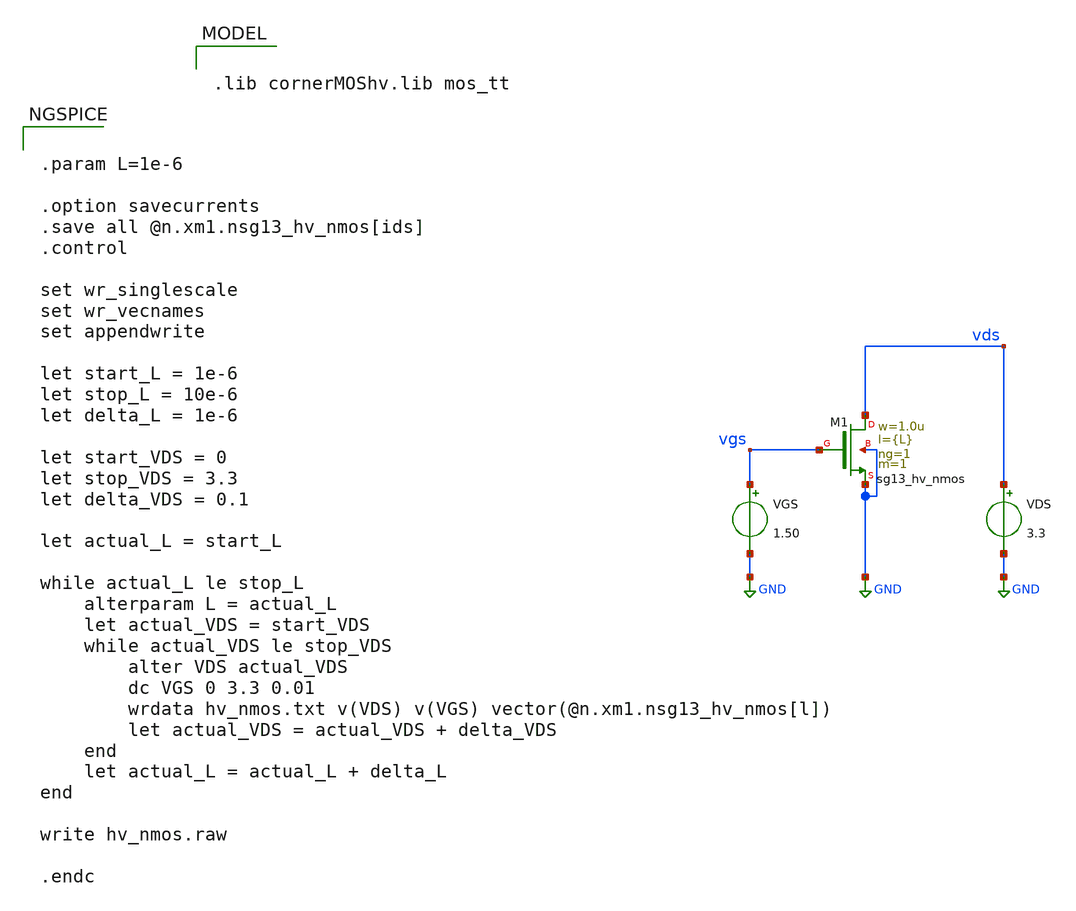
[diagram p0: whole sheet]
** sch_path: gmid/hv_nmos.sch
**.subckt hv_nmos
XM1 vds vgs GND GND sg13_hv_nmos w=1.0u l={L} ng=1 m=1 mm_ok=1
VGS vgs GND 1.50
VDS vds GND 3.3
**** begin user architecture code

.lib cornerMOShv.lib mos_tt



.param L=1e-6

.option savecurrents
.save all @n.xm1.nsg13_hv_nmos[ids]
.control

set wr_singlescale
set wr_vecnames
set appendwrite

let start_L = 1e-6
let stop_L = 10e-6
let delta_L = 1e-6

let start_VDS = 0
let stop_VDS = 3.3
let delta_VDS = 0.1

let actual_L = start_L

while actual_L le stop_L
	alterparam L = actual_L
	let actual_VDS = start_VDS
	while actual_VDS le stop_VDS
		alter VDS actual_VDS
		dc VGS 0 3.3 0.01
		wrdata hv_nmos.txt v(VDS) v(VGS) vector(@n.xm1.nsg13_hv_nmos[l])
		let actual_VDS = actual_VDS + delta_VDS
	end
	let actual_L = actual_L + delta_L
end

write hv_nmos.raw

.endc



**** end user architecture code
**.ends
.GLOBAL GND
.end
